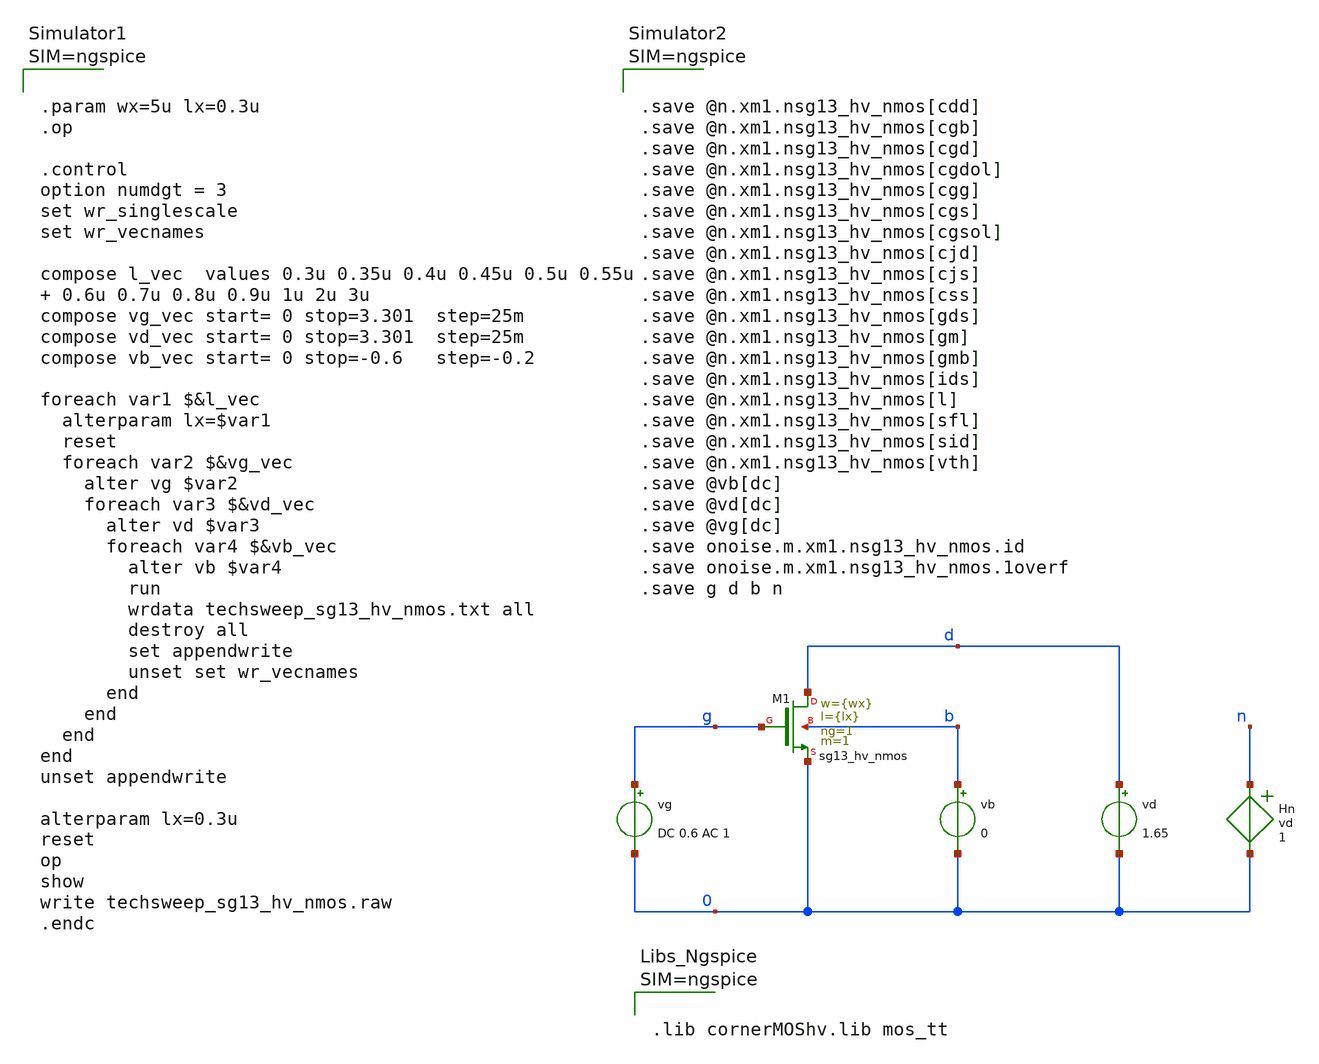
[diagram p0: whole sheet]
** sch_path: starter_files_open_source_tools/ihp-sg13cmos5l/techsweep_sg13_hv_nmos.sch
**.subckt techsweep_sg13_hv_nmos
vg g 0 DC 0.6 AC 1
vb b 0 0
vd d 0 1.65
Hn n 0 vd 1
XM1 d g 0 b sg13_hv_nmos w={wx} l={lx} ng=1 m=1 mm_ok=1
**** begin user architecture code



.lib cornerMOShv.lib mos_tt






.save @n.xm1.nsg13_hv_nmos[cdd]
.save @n.xm1.nsg13_hv_nmos[cgb]
.save @n.xm1.nsg13_hv_nmos[cgd]
.save @n.xm1.nsg13_hv_nmos[cgdol]
.save @n.xm1.nsg13_hv_nmos[cgg]
.save @n.xm1.nsg13_hv_nmos[cgs]
.save @n.xm1.nsg13_hv_nmos[cgsol]
.save @n.xm1.nsg13_hv_nmos[cjd]
.save @n.xm1.nsg13_hv_nmos[cjs]
.save @n.xm1.nsg13_hv_nmos[css]
.save @n.xm1.nsg13_hv_nmos[gds]
.save @n.xm1.nsg13_hv_nmos[gm]
.save @n.xm1.nsg13_hv_nmos[gmb]
.save @n.xm1.nsg13_hv_nmos[ids]
.save @n.xm1.nsg13_hv_nmos[l]
.save @n.xm1.nsg13_hv_nmos[sfl]
.save @n.xm1.nsg13_hv_nmos[sid]
.save @n.xm1.nsg13_hv_nmos[vth]
.save @vb[dc]
.save @vd[dc]
.save @vg[dc]
.save onoise.m.xm1.nsg13_hv_nmos.id
.save onoise.m.xm1.nsg13_hv_nmos.1overf
.save g d b n






.param wx=5u lx=0.3u
.op

.control
option numdgt = 3
set wr_singlescale
set wr_vecnames

compose l_vec  values 0.3u 0.35u 0.4u 0.45u 0.5u 0.55u  0.6u 0.7u 0.8u 0.9u 1u 2u 3u
compose vg_vec start= 0 stop=3.301  step=25m
compose vd_vec start= 0 stop=3.301  step=25m
compose vb_vec start= 0 stop=-0.6   step=-0.2

foreach var1 $&l_vec
  alterparam lx=$var1
  reset
  foreach var2 $&vg_vec
    alter vg $var2
    foreach var3 $&vd_vec
      alter vd $var3
      foreach var4 $&vb_vec
        alter vb $var4
        run
        wrdata techsweep_sg13_hv_nmos.txt all
        destroy all
        set appendwrite
        unset set wr_vecnames
      end
    end
  end
end
unset appendwrite

alterparam lx=0.3u
reset
op
show
write techsweep_sg13_hv_nmos.raw
.endc



**** end user architecture code
**.ends
.end
